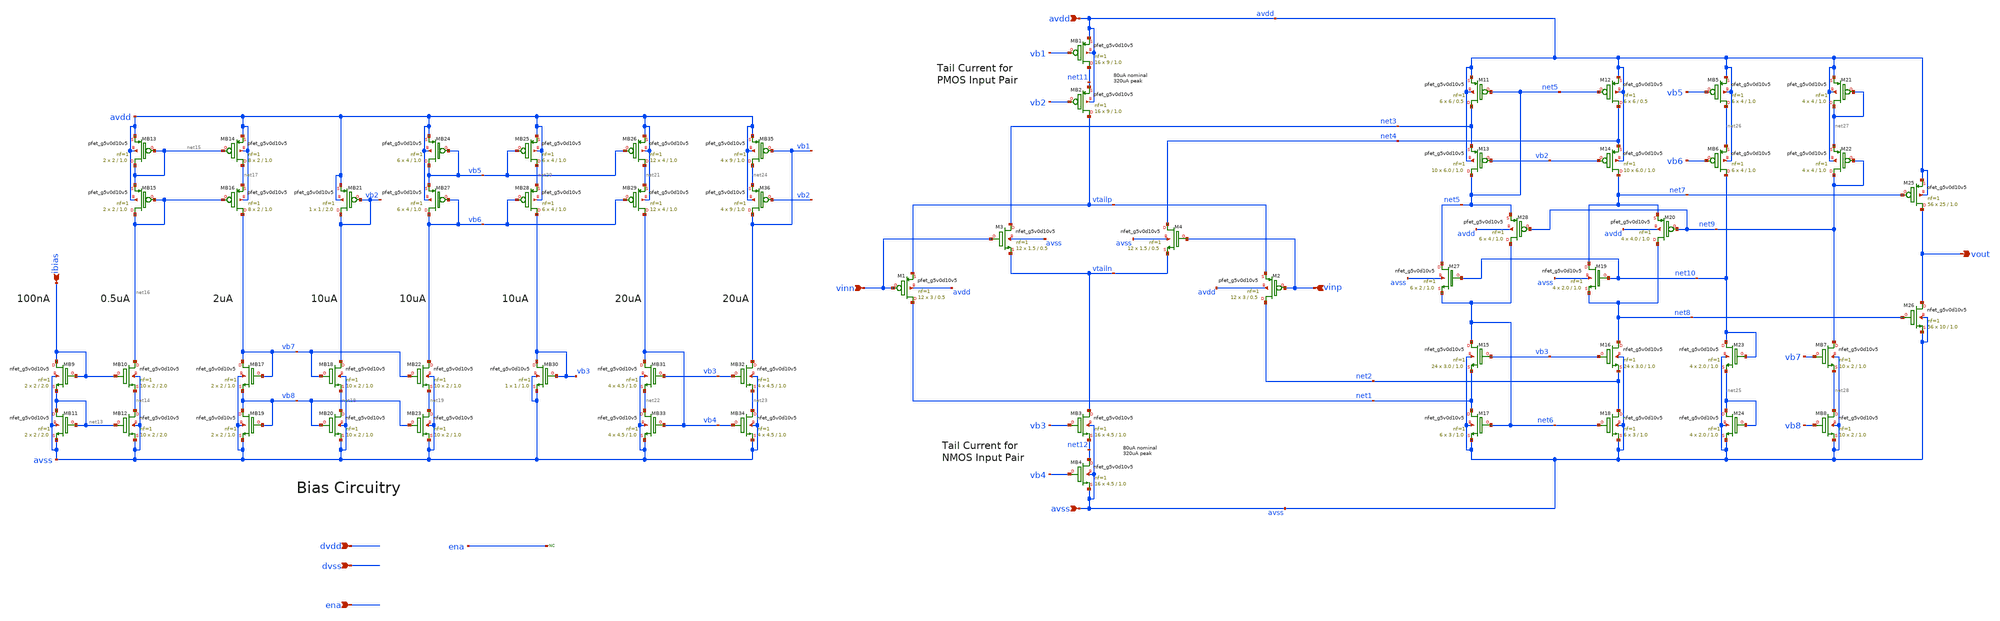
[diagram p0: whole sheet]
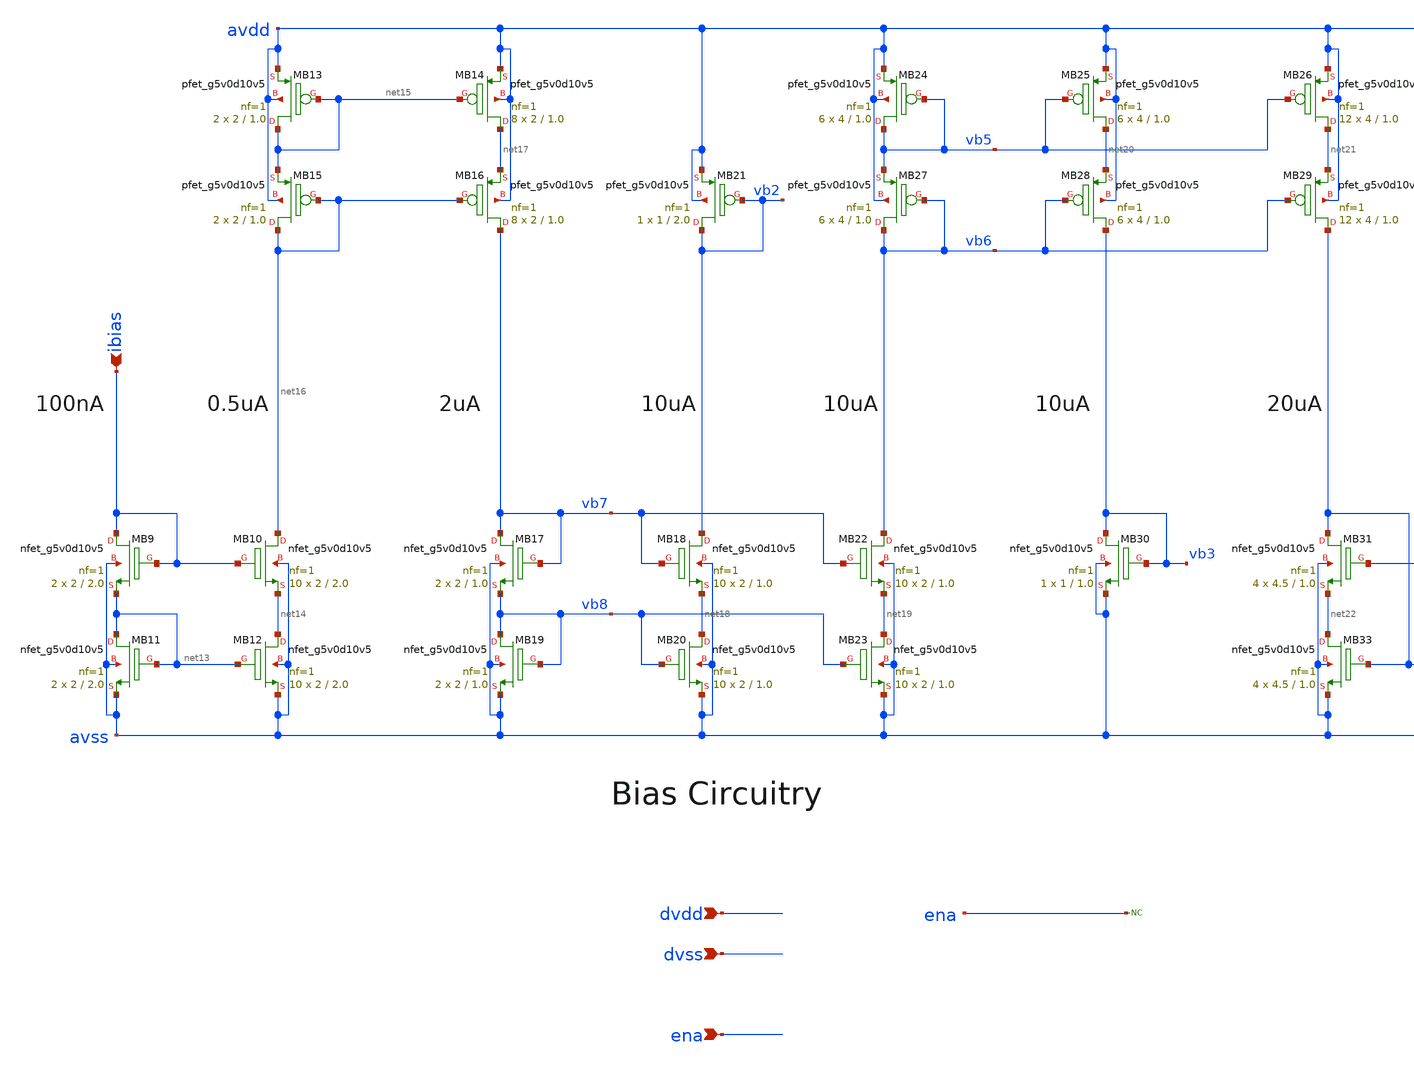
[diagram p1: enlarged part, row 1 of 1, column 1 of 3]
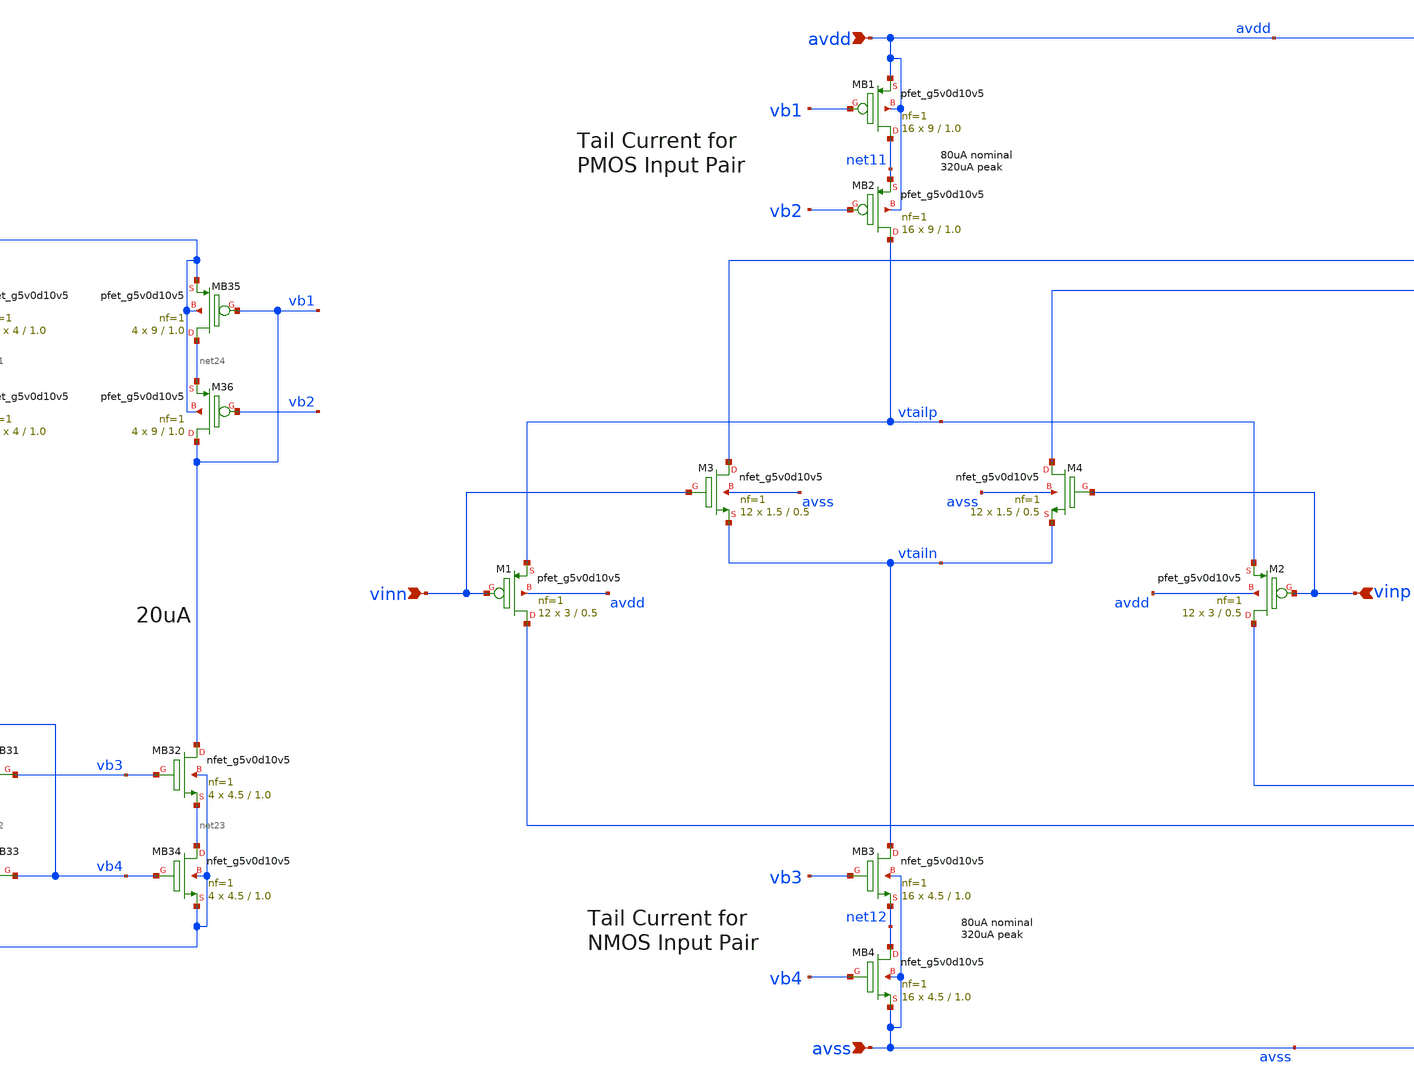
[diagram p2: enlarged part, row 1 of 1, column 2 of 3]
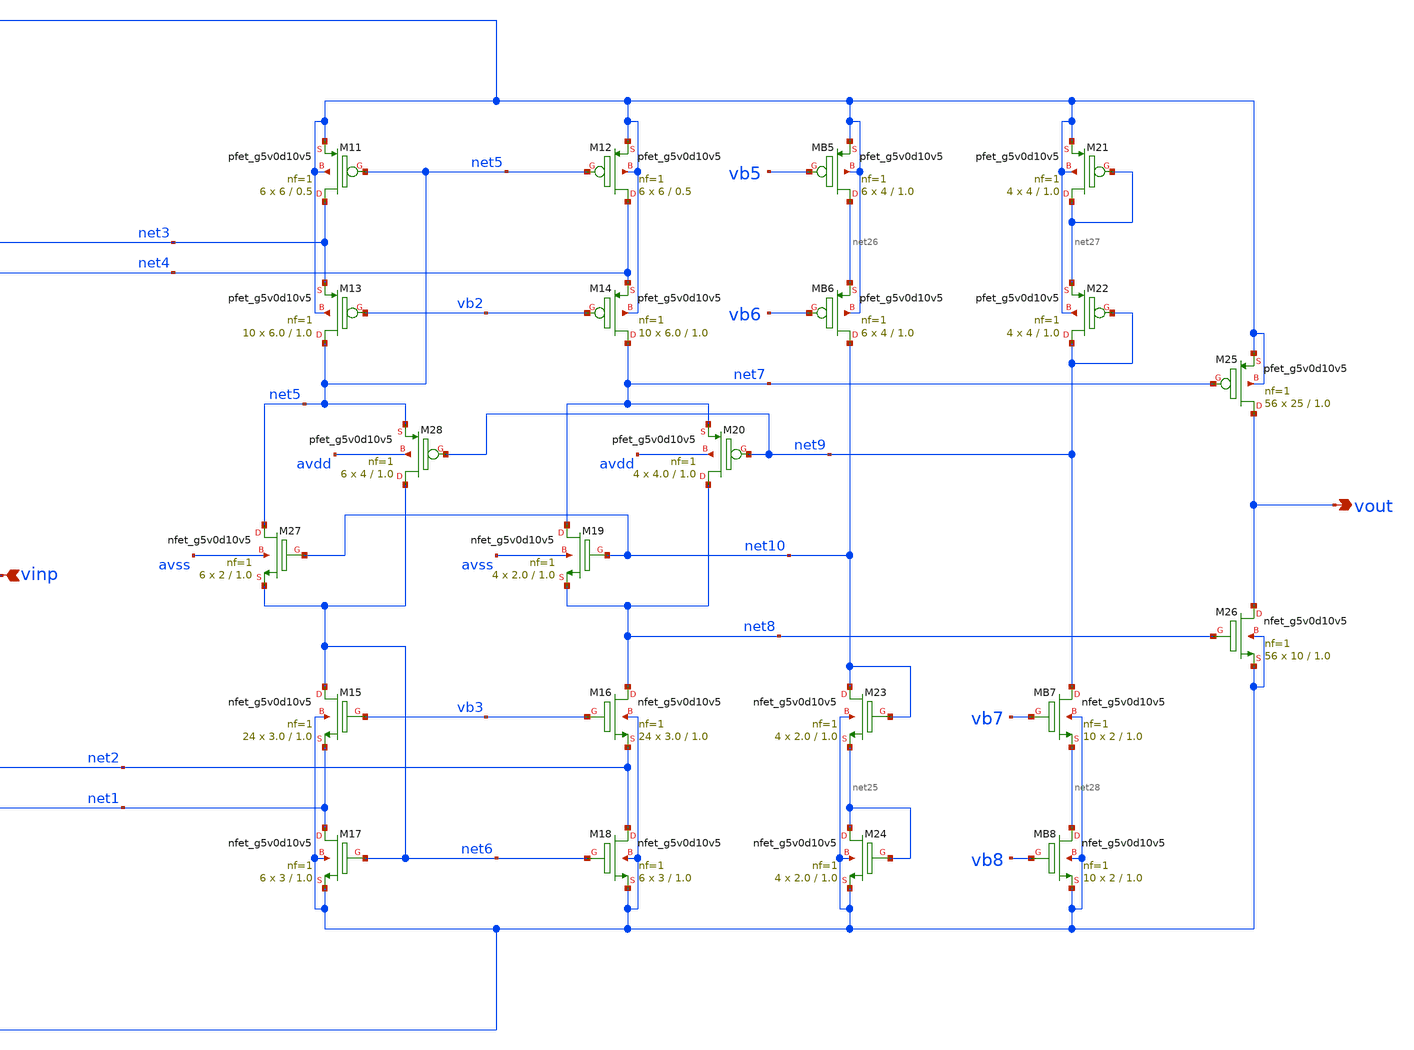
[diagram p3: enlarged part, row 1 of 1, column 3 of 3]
** sch_path: xschem/sky130_td_ip__opamp_hp.sch
**.subckt sky130_td_ip__opamp_hp vinn vinp vout ena ibias avss avdd dvdd dvss
*.ipin vinn
*.ipin vinp
*.opin vout
*.ipin ena
*.ipin ibias
*.ipin avss
*.ipin avdd
*.ipin dvdd
*.ipin dvss
XM3 net3 vinn vtailn avss sky130_fd_pr__nfet_g5v0d10v5 L=0.5 W=1.5 nf=1 ad='int((nf+1)/2) * W/nf * 0.29'
+ as='int((nf+2)/2) * W/nf * 0.29' pd='2*int((nf+1)/2) * (W/nf + 0.29)' ps='2*int((nf+2)/2) * (W/nf + 0.29)'
+ nrd='0.29 / W' nrs='0.29 / W' sa=0 sb=0 sd=0 mult=12 m=12
XM4 net4 vinp vtailn avss sky130_fd_pr__nfet_g5v0d10v5 L=0.5 W=1.5 nf=1 ad='int((nf+1)/2) * W/nf * 0.29'
+ as='int((nf+2)/2) * W/nf * 0.29' pd='2*int((nf+1)/2) * (W/nf + 0.29)' ps='2*int((nf+2)/2) * (W/nf + 0.29)'
+ nrd='0.29 / W' nrs='0.29 / W' sa=0 sb=0 sd=0 mult=12 m=12
XMB3 vtailn vb3 net12 avss sky130_fd_pr__nfet_g5v0d10v5 L=1.0 W=4.5 nf=1 ad='int((nf+1)/2) * W/nf * 0.29'
+ as='int((nf+2)/2) * W/nf * 0.29' pd='2*int((nf+1)/2) * (W/nf + 0.29)' ps='2*int((nf+2)/2) * (W/nf + 0.29)'
+ nrd='0.29 / W' nrs='0.29 / W' sa=0 sb=0 sd=0 mult=16 m=16
XMB4 net12 vb4 avss avss sky130_fd_pr__nfet_g5v0d10v5 L=1.0 W=4.5 nf=1 ad='int((nf+1)/2) * W/nf * 0.29'
+ as='int((nf+2)/2) * W/nf * 0.29' pd='2*int((nf+1)/2) * (W/nf + 0.29)' ps='2*int((nf+2)/2) * (W/nf + 0.29)'
+ nrd='0.29 / W' nrs='0.29 / W' sa=0 sb=0 sd=0 mult=16 m=16
XM1 net1 vinn vtailp avdd sky130_fd_pr__pfet_g5v0d10v5 L=0.5 W=3 nf=1 ad='int((nf+1)/2) * W/nf * 0.29'
+ as='int((nf+2)/2) * W/nf * 0.29' pd='2*int((nf+1)/2) * (W/nf + 0.29)' ps='2*int((nf+2)/2) * (W/nf + 0.29)'
+ nrd='0.29 / W' nrs='0.29 / W' sa=0 sb=0 sd=0 mult=12 m=12
XM2 net2 vinp vtailp avdd sky130_fd_pr__pfet_g5v0d10v5 L=0.5 W=3 nf=1 ad='int((nf+1)/2) * W/nf * 0.29'
+ as='int((nf+2)/2) * W/nf * 0.29' pd='2*int((nf+1)/2) * (W/nf + 0.29)' ps='2*int((nf+2)/2) * (W/nf + 0.29)'
+ nrd='0.29 / W' nrs='0.29 / W' sa=0 sb=0 sd=0 mult=12 m=12
XMB2 vtailp vb2 net11 avdd sky130_fd_pr__pfet_g5v0d10v5 L=1.0 W=9 nf=1 ad='int((nf+1)/2) * W/nf * 0.29'
+ as='int((nf+2)/2) * W/nf * 0.29' pd='2*int((nf+1)/2) * (W/nf + 0.29)' ps='2*int((nf+2)/2) * (W/nf + 0.29)'
+ nrd='0.29 / W' nrs='0.29 / W' sa=0 sb=0 sd=0 mult=16 m=16
XMB1 net11 vb1 avdd avdd sky130_fd_pr__pfet_g5v0d10v5 L=1.0 W=9 nf=1 ad='int((nf+1)/2) * W/nf * 0.29'
+ as='int((nf+2)/2) * W/nf * 0.29' pd='2*int((nf+1)/2) * (W/nf + 0.29)' ps='2*int((nf+2)/2) * (W/nf + 0.29)'
+ nrd='0.29 / W' nrs='0.29 / W' sa=0 sb=0 sd=0 mult=16 m=16
XM12 net4 net5 avdd avdd sky130_fd_pr__pfet_g5v0d10v5 L=0.5 W=6 nf=1 ad='int((nf+1)/2) * W/nf * 0.29'
+ as='int((nf+2)/2) * W/nf * 0.29' pd='2*int((nf+1)/2) * (W/nf + 0.29)' ps='2*int((nf+2)/2) * (W/nf + 0.29)'
+ nrd='0.29 / W' nrs='0.29 / W' sa=0 sb=0 sd=0 mult=6 m=6
XM11 net3 net5 avdd avdd sky130_fd_pr__pfet_g5v0d10v5 L=0.5 W=6 nf=1 ad='int((nf+1)/2) * W/nf * 0.29'
+ as='int((nf+2)/2) * W/nf * 0.29' pd='2*int((nf+1)/2) * (W/nf + 0.29)' ps='2*int((nf+2)/2) * (W/nf + 0.29)'
+ nrd='0.29 / W' nrs='0.29 / W' sa=0 sb=0 sd=0 mult=6 m=6
XM14 net7 vb2 net4 avdd sky130_fd_pr__pfet_g5v0d10v5 L=1.0 W=6.0 nf=1 ad='int((nf+1)/2) * W/nf * 0.29'
+ as='int((nf+2)/2) * W/nf * 0.29' pd='2*int((nf+1)/2) * (W/nf + 0.29)' ps='2*int((nf+2)/2) * (W/nf + 0.29)'
+ nrd='0.29 / W' nrs='0.29 / W' sa=0 sb=0 sd=0 mult=10 m=10
XM13 net5 vb2 net3 avdd sky130_fd_pr__pfet_g5v0d10v5 L=1.0 W=6.0 nf=1 ad='int((nf+1)/2) * W/nf * 0.29'
+ as='int((nf+2)/2) * W/nf * 0.29' pd='2*int((nf+1)/2) * (W/nf + 0.29)' ps='2*int((nf+2)/2) * (W/nf + 0.29)'
+ nrd='0.29 / W' nrs='0.29 / W' sa=0 sb=0 sd=0 mult=10 m=10
XM18 net2 net6 avss avss sky130_fd_pr__nfet_g5v0d10v5 L=1.0 W=3 nf=1 ad='int((nf+1)/2) * W/nf * 0.29'
+ as='int((nf+2)/2) * W/nf * 0.29' pd='2*int((nf+1)/2) * (W/nf + 0.29)' ps='2*int((nf+2)/2) * (W/nf + 0.29)'
+ nrd='0.29 / W' nrs='0.29 / W' sa=0 sb=0 sd=0 mult=6 m=6
XM16 net8 vb3 net2 avss sky130_fd_pr__nfet_g5v0d10v5 L=1.0 W=3.0 nf=1 ad='int((nf+1)/2) * W/nf * 0.29'
+ as='int((nf+2)/2) * W/nf * 0.29' pd='2*int((nf+1)/2) * (W/nf + 0.29)' ps='2*int((nf+2)/2) * (W/nf + 0.29)'
+ nrd='0.29 / W' nrs='0.29 / W' sa=0 sb=0 sd=0 mult=24 m=24
XM17 net1 net6 avss avss sky130_fd_pr__nfet_g5v0d10v5 L=1.0 W=3 nf=1 ad='int((nf+1)/2) * W/nf * 0.29'
+ as='int((nf+2)/2) * W/nf * 0.29' pd='2*int((nf+1)/2) * (W/nf + 0.29)' ps='2*int((nf+2)/2) * (W/nf + 0.29)'
+ nrd='0.29 / W' nrs='0.29 / W' sa=0 sb=0 sd=0 mult=6 m=6
XM15 net6 vb3 net1 avss sky130_fd_pr__nfet_g5v0d10v5 L=1.0 W=3.0 nf=1 ad='int((nf+1)/2) * W/nf * 0.29'
+ as='int((nf+2)/2) * W/nf * 0.29' pd='2*int((nf+1)/2) * (W/nf + 0.29)' ps='2*int((nf+2)/2) * (W/nf + 0.29)'
+ nrd='0.29 / W' nrs='0.29 / W' sa=0 sb=0 sd=0 mult=24 m=24
XM28 net6 net9 net5 avdd sky130_fd_pr__pfet_g5v0d10v5 L=1.0 W=4 nf=1 ad='int((nf+1)/2) * W/nf * 0.29'
+ as='int((nf+2)/2) * W/nf * 0.29' pd='2*int((nf+1)/2) * (W/nf + 0.29)' ps='2*int((nf+2)/2) * (W/nf + 0.29)'
+ nrd='0.29 / W' nrs='0.29 / W' sa=0 sb=0 sd=0 mult=6 m=6
XM27 net5 net10 net6 avss sky130_fd_pr__nfet_g5v0d10v5 L=1.0 W=2 nf=1 ad='int((nf+1)/2) * W/nf * 0.29'
+ as='int((nf+2)/2) * W/nf * 0.29' pd='2*int((nf+1)/2) * (W/nf + 0.29)' ps='2*int((nf+2)/2) * (W/nf + 0.29)'
+ nrd='0.29 / W' nrs='0.29 / W' sa=0 sb=0 sd=0 mult=6 m=6
XM20 net8 net9 net7 avdd sky130_fd_pr__pfet_g5v0d10v5 L=1.0 W=4.0 nf=1 ad='int((nf+1)/2) * W/nf * 0.29'
+ as='int((nf+2)/2) * W/nf * 0.29' pd='2*int((nf+1)/2) * (W/nf + 0.29)' ps='2*int((nf+2)/2) * (W/nf + 0.29)'
+ nrd='0.29 / W' nrs='0.29 / W' sa=0 sb=0 sd=0 mult=4 m=4
XM19 net7 net10 net8 avss sky130_fd_pr__nfet_g5v0d10v5 L=1.0 W=2.0 nf=1 ad='int((nf+1)/2) * W/nf * 0.29'
+ as='int((nf+2)/2) * W/nf * 0.29' pd='2*int((nf+1)/2) * (W/nf + 0.29)' ps='2*int((nf+2)/2) * (W/nf + 0.29)'
+ nrd='0.29 / W' nrs='0.29 / W' sa=0 sb=0 sd=0 mult=4 m=4
XM26 vout net8 avss avss sky130_fd_pr__nfet_g5v0d10v5 L=1.0 W=10 nf=1 ad='int((nf+1)/2) * W/nf * 0.29'
+ as='int((nf+2)/2) * W/nf * 0.29' pd='2*int((nf+1)/2) * (W/nf + 0.29)' ps='2*int((nf+2)/2) * (W/nf + 0.29)'
+ nrd='0.29 / W' nrs='0.29 / W' sa=0 sb=0 sd=0 mult=56 m=56
XM25 vout net7 avdd avdd sky130_fd_pr__pfet_g5v0d10v5 L=1.0 W=25 nf=1 ad='int((nf+1)/2) * W/nf * 0.29'
+ as='int((nf+2)/2) * W/nf * 0.29' pd='2*int((nf+1)/2) * (W/nf + 0.29)' ps='2*int((nf+2)/2) * (W/nf + 0.29)'
+ nrd='0.29 / W' nrs='0.29 / W' sa=0 sb=0 sd=0 mult=56 m=56
XMB9 ibias ibias net13 avss sky130_fd_pr__nfet_g5v0d10v5 L=2.0 W=2 nf=1 ad='int((nf+1)/2) * W/nf * 0.29'
+ as='int((nf+2)/2) * W/nf * 0.29' pd='2*int((nf+1)/2) * (W/nf + 0.29)' ps='2*int((nf+2)/2) * (W/nf + 0.29)'
+ nrd='0.29 / W' nrs='0.29 / W' sa=0 sb=0 sd=0 mult=2 m=2
XMB11 net13 net13 avss avss sky130_fd_pr__nfet_g5v0d10v5 L=2.0 W=2 nf=1 ad='int((nf+1)/2) * W/nf * 0.29'
+ as='int((nf+2)/2) * W/nf * 0.29' pd='2*int((nf+1)/2) * (W/nf + 0.29)' ps='2*int((nf+2)/2) * (W/nf + 0.29)'
+ nrd='0.29 / W' nrs='0.29 / W' sa=0 sb=0 sd=0 mult=2 m=2
XMB10 net16 ibias net14 avss sky130_fd_pr__nfet_g5v0d10v5 L=2.0 W=2 nf=1 ad='int((nf+1)/2) * W/nf * 0.29'
+ as='int((nf+2)/2) * W/nf * 0.29' pd='2*int((nf+1)/2) * (W/nf + 0.29)' ps='2*int((nf+2)/2) * (W/nf + 0.29)'
+ nrd='0.29 / W' nrs='0.29 / W' sa=0 sb=0 sd=0 mult=10 m=10
XMB12 net14 net13 avss avss sky130_fd_pr__nfet_g5v0d10v5 L=2.0 W=2 nf=1 ad='int((nf+1)/2) * W/nf * 0.29'
+ as='int((nf+2)/2) * W/nf * 0.29' pd='2*int((nf+1)/2) * (W/nf + 0.29)' ps='2*int((nf+2)/2) * (W/nf + 0.29)'
+ nrd='0.29 / W' nrs='0.29 / W' sa=0 sb=0 sd=0 mult=10 m=10
XMB15 net16 net16 net15 avdd sky130_fd_pr__pfet_g5v0d10v5 L=1.0 W=2 nf=1 ad='int((nf+1)/2) * W/nf * 0.29'
+ as='int((nf+2)/2) * W/nf * 0.29' pd='2*int((nf+1)/2) * (W/nf + 0.29)' ps='2*int((nf+2)/2) * (W/nf + 0.29)'
+ nrd='0.29 / W' nrs='0.29 / W' sa=0 sb=0 sd=0 mult=2 m=2
XMB13 net15 net15 avdd avdd sky130_fd_pr__pfet_g5v0d10v5 L=1.0 W=2 nf=1 ad='int((nf+1)/2) * W/nf * 0.29'
+ as='int((nf+2)/2) * W/nf * 0.29' pd='2*int((nf+1)/2) * (W/nf + 0.29)' ps='2*int((nf+2)/2) * (W/nf + 0.29)'
+ nrd='0.29 / W' nrs='0.29 / W' sa=0 sb=0 sd=0 mult=2 m=2
XMB16 vb7 net16 net17 avdd sky130_fd_pr__pfet_g5v0d10v5 L=1.0 W=2 nf=1 ad='int((nf+1)/2) * W/nf * 0.29'
+ as='int((nf+2)/2) * W/nf * 0.29' pd='2*int((nf+1)/2) * (W/nf + 0.29)' ps='2*int((nf+2)/2) * (W/nf + 0.29)'
+ nrd='0.29 / W' nrs='0.29 / W' sa=0 sb=0 sd=0 mult=8 m=8
XMB14 net17 net15 avdd avdd sky130_fd_pr__pfet_g5v0d10v5 L=1.0 W=2 nf=1 ad='int((nf+1)/2) * W/nf * 0.29'
+ as='int((nf+2)/2) * W/nf * 0.29' pd='2*int((nf+1)/2) * (W/nf + 0.29)' ps='2*int((nf+2)/2) * (W/nf + 0.29)'
+ nrd='0.29 / W' nrs='0.29 / W' sa=0 sb=0 sd=0 mult=8 m=8
XMB17 vb7 vb7 vb8 avss sky130_fd_pr__nfet_g5v0d10v5 L=1.0 W=2 nf=1 ad='int((nf+1)/2) * W/nf * 0.29' as='int((nf+2)/2) * W/nf * 0.29'
+ pd='2*int((nf+1)/2) * (W/nf + 0.29)' ps='2*int((nf+2)/2) * (W/nf + 0.29)' nrd='0.29 / W' nrs='0.29 / W'
+ sa=0 sb=0 sd=0 mult=2 m=2
XMB19 vb8 vb8 avss avss sky130_fd_pr__nfet_g5v0d10v5 L=1.0 W=2 nf=1 ad='int((nf+1)/2) * W/nf * 0.29'
+ as='int((nf+2)/2) * W/nf * 0.29' pd='2*int((nf+1)/2) * (W/nf + 0.29)' ps='2*int((nf+2)/2) * (W/nf + 0.29)'
+ nrd='0.29 / W' nrs='0.29 / W' sa=0 sb=0 sd=0 mult=2 m=2
XMB18 vb2 vb7 net18 avss sky130_fd_pr__nfet_g5v0d10v5 L=1.0 W=2 nf=1 ad='int((nf+1)/2) * W/nf * 0.29'
+ as='int((nf+2)/2) * W/nf * 0.29' pd='2*int((nf+1)/2) * (W/nf + 0.29)' ps='2*int((nf+2)/2) * (W/nf + 0.29)'
+ nrd='0.29 / W' nrs='0.29 / W' sa=0 sb=0 sd=0 mult=10 m=10
XMB20 net18 vb8 avss avss sky130_fd_pr__nfet_g5v0d10v5 L=1.0 W=2 nf=1 ad='int((nf+1)/2) * W/nf * 0.29'
+ as='int((nf+2)/2) * W/nf * 0.29' pd='2*int((nf+1)/2) * (W/nf + 0.29)' ps='2*int((nf+2)/2) * (W/nf + 0.29)'
+ nrd='0.29 / W' nrs='0.29 / W' sa=0 sb=0 sd=0 mult=10 m=10
XMB22 vb6 vb7 net19 avss sky130_fd_pr__nfet_g5v0d10v5 L=1.0 W=2 nf=1 ad='int((nf+1)/2) * W/nf * 0.29'
+ as='int((nf+2)/2) * W/nf * 0.29' pd='2*int((nf+1)/2) * (W/nf + 0.29)' ps='2*int((nf+2)/2) * (W/nf + 0.29)'
+ nrd='0.29 / W' nrs='0.29 / W' sa=0 sb=0 sd=0 mult=10 m=10
XMB23 net19 vb8 avss avss sky130_fd_pr__nfet_g5v0d10v5 L=1.0 W=2 nf=1 ad='int((nf+1)/2) * W/nf * 0.29'
+ as='int((nf+2)/2) * W/nf * 0.29' pd='2*int((nf+1)/2) * (W/nf + 0.29)' ps='2*int((nf+2)/2) * (W/nf + 0.29)'
+ nrd='0.29 / W' nrs='0.29 / W' sa=0 sb=0 sd=0 mult=10 m=10
XMB21 vb2 vb2 avdd avdd sky130_fd_pr__pfet_g5v0d10v5 L=2.0 W=1 nf=1 ad='int((nf+1)/2) * W/nf * 0.29'
+ as='int((nf+2)/2) * W/nf * 0.29' pd='2*int((nf+1)/2) * (W/nf + 0.29)' ps='2*int((nf+2)/2) * (W/nf + 0.29)'
+ nrd='0.29 / W' nrs='0.29 / W' sa=0 sb=0 sd=0 mult=1 m=1
XMB27 vb6 vb6 vb5 avdd sky130_fd_pr__pfet_g5v0d10v5 L=1.0 W=4 nf=1 ad='int((nf+1)/2) * W/nf * 0.29' as='int((nf+2)/2) * W/nf * 0.29'
+ pd='2*int((nf+1)/2) * (W/nf + 0.29)' ps='2*int((nf+2)/2) * (W/nf + 0.29)' nrd='0.29 / W' nrs='0.29 / W'
+ sa=0 sb=0 sd=0 mult=6 m=6
XMB24 vb5 vb5 avdd avdd sky130_fd_pr__pfet_g5v0d10v5 L=1.0 W=4 nf=1 ad='int((nf+1)/2) * W/nf * 0.29'
+ as='int((nf+2)/2) * W/nf * 0.29' pd='2*int((nf+1)/2) * (W/nf + 0.29)' ps='2*int((nf+2)/2) * (W/nf + 0.29)'
+ nrd='0.29 / W' nrs='0.29 / W' sa=0 sb=0 sd=0 mult=6 m=6
XMB28 vb3 vb6 net20 avdd sky130_fd_pr__pfet_g5v0d10v5 L=1.0 W=4 nf=1 ad='int((nf+1)/2) * W/nf * 0.29'
+ as='int((nf+2)/2) * W/nf * 0.29' pd='2*int((nf+1)/2) * (W/nf + 0.29)' ps='2*int((nf+2)/2) * (W/nf + 0.29)'
+ nrd='0.29 / W' nrs='0.29 / W' sa=0 sb=0 sd=0 mult=6 m=6
XMB25 net20 vb5 avdd avdd sky130_fd_pr__pfet_g5v0d10v5 L=1.0 W=4 nf=1 ad='int((nf+1)/2) * W/nf * 0.29'
+ as='int((nf+2)/2) * W/nf * 0.29' pd='2*int((nf+1)/2) * (W/nf + 0.29)' ps='2*int((nf+2)/2) * (W/nf + 0.29)'
+ nrd='0.29 / W' nrs='0.29 / W' sa=0 sb=0 sd=0 mult=6 m=6
XMB29 vb4 vb6 net21 avdd sky130_fd_pr__pfet_g5v0d10v5 L=1.0 W=4 nf=1 ad='int((nf+1)/2) * W/nf * 0.29'
+ as='int((nf+2)/2) * W/nf * 0.29' pd='2*int((nf+1)/2) * (W/nf + 0.29)' ps='2*int((nf+2)/2) * (W/nf + 0.29)'
+ nrd='0.29 / W' nrs='0.29 / W' sa=0 sb=0 sd=0 mult=12 m=12
XMB26 net21 vb5 avdd avdd sky130_fd_pr__pfet_g5v0d10v5 L=1.0 W=4 nf=1 ad='int((nf+1)/2) * W/nf * 0.29'
+ as='int((nf+2)/2) * W/nf * 0.29' pd='2*int((nf+1)/2) * (W/nf + 0.29)' ps='2*int((nf+2)/2) * (W/nf + 0.29)'
+ nrd='0.29 / W' nrs='0.29 / W' sa=0 sb=0 sd=0 mult=12 m=12
XMB30 vb3 vb3 avss avss sky130_fd_pr__nfet_g5v0d10v5 L=1.0 W=1 nf=1 ad='int((nf+1)/2) * W/nf * 0.29'
+ as='int((nf+2)/2) * W/nf * 0.29' pd='2*int((nf+1)/2) * (W/nf + 0.29)' ps='2*int((nf+2)/2) * (W/nf + 0.29)'
+ nrd='0.29 / W' nrs='0.29 / W' sa=0 sb=0 sd=0 mult=1 m=1
XMB31 vb4 vb3 net22 avss sky130_fd_pr__nfet_g5v0d10v5 L=1.0 W=4.5 nf=1 ad='int((nf+1)/2) * W/nf * 0.29'
+ as='int((nf+2)/2) * W/nf * 0.29' pd='2*int((nf+1)/2) * (W/nf + 0.29)' ps='2*int((nf+2)/2) * (W/nf + 0.29)'
+ nrd='0.29 / W' nrs='0.29 / W' sa=0 sb=0 sd=0 mult=4 m=4
XMB33 net22 vb4 avss avss sky130_fd_pr__nfet_g5v0d10v5 L=1.0 W=4.5 nf=1 ad='int((nf+1)/2) * W/nf * 0.29'
+ as='int((nf+2)/2) * W/nf * 0.29' pd='2*int((nf+1)/2) * (W/nf + 0.29)' ps='2*int((nf+2)/2) * (W/nf + 0.29)'
+ nrd='0.29 / W' nrs='0.29 / W' sa=0 sb=0 sd=0 mult=4 m=4
XMB32 vb1 vb3 net23 avss sky130_fd_pr__nfet_g5v0d10v5 L=1.0 W=4.5 nf=1 ad='int((nf+1)/2) * W/nf * 0.29'
+ as='int((nf+2)/2) * W/nf * 0.29' pd='2*int((nf+1)/2) * (W/nf + 0.29)' ps='2*int((nf+2)/2) * (W/nf + 0.29)'
+ nrd='0.29 / W' nrs='0.29 / W' sa=0 sb=0 sd=0 mult=4 m=4
XMB34 net23 vb4 avss avss sky130_fd_pr__nfet_g5v0d10v5 L=1.0 W=4.5 nf=1 ad='int((nf+1)/2) * W/nf * 0.29'
+ as='int((nf+2)/2) * W/nf * 0.29' pd='2*int((nf+1)/2) * (W/nf + 0.29)' ps='2*int((nf+2)/2) * (W/nf + 0.29)'
+ nrd='0.29 / W' nrs='0.29 / W' sa=0 sb=0 sd=0 mult=4 m=4
XM36 vb1 vb2 net24 avdd sky130_fd_pr__pfet_g5v0d10v5 L=1.0 W=9 nf=1 ad='int((nf+1)/2) * W/nf * 0.29'
+ as='int((nf+2)/2) * W/nf * 0.29' pd='2*int((nf+1)/2) * (W/nf + 0.29)' ps='2*int((nf+2)/2) * (W/nf + 0.29)'
+ nrd='0.29 / W' nrs='0.29 / W' sa=0 sb=0 sd=0 mult=4 m=4
XMB35 net24 vb1 avdd avdd sky130_fd_pr__pfet_g5v0d10v5 L=1.0 W=9 nf=1 ad='int((nf+1)/2) * W/nf * 0.29'
+ as='int((nf+2)/2) * W/nf * 0.29' pd='2*int((nf+1)/2) * (W/nf + 0.29)' ps='2*int((nf+2)/2) * (W/nf + 0.29)'
+ nrd='0.29 / W' nrs='0.29 / W' sa=0 sb=0 sd=0 mult=4 m=4
XM24 net25 net25 avss avss sky130_fd_pr__nfet_g5v0d10v5 L=1.0 W=2.0 nf=1 ad='int((nf+1)/2) * W/nf * 0.29'
+ as='int((nf+2)/2) * W/nf * 0.29' pd='2*int((nf+1)/2) * (W/nf + 0.29)' ps='2*int((nf+2)/2) * (W/nf + 0.29)'
+ nrd='0.29 / W' nrs='0.29 / W' sa=0 sb=0 sd=0 mult=4 m=4
XM23 net10 net10 net25 avss sky130_fd_pr__nfet_g5v0d10v5 L=1.0 W=2.0 nf=1 ad='int((nf+1)/2) * W/nf * 0.29'
+ as='int((nf+2)/2) * W/nf * 0.29' pd='2*int((nf+1)/2) * (W/nf + 0.29)' ps='2*int((nf+2)/2) * (W/nf + 0.29)'
+ nrd='0.29 / W' nrs='0.29 / W' sa=0 sb=0 sd=0 mult=4 m=4
XMB5 net26 vb5 avdd avdd sky130_fd_pr__pfet_g5v0d10v5 L=1.0 W=4 nf=1 ad='int((nf+1)/2) * W/nf * 0.29'
+ as='int((nf+2)/2) * W/nf * 0.29' pd='2*int((nf+1)/2) * (W/nf + 0.29)' ps='2*int((nf+2)/2) * (W/nf + 0.29)'
+ nrd='0.29 / W' nrs='0.29 / W' sa=0 sb=0 sd=0 mult=6 m=6
XMB6 net10 vb6 net26 avdd sky130_fd_pr__pfet_g5v0d10v5 L=1.0 W=4 nf=1 ad='int((nf+1)/2) * W/nf * 0.29'
+ as='int((nf+2)/2) * W/nf * 0.29' pd='2*int((nf+1)/2) * (W/nf + 0.29)' ps='2*int((nf+2)/2) * (W/nf + 0.29)'
+ nrd='0.29 / W' nrs='0.29 / W' sa=0 sb=0 sd=0 mult=6 m=6
XM21 net27 net27 avdd avdd sky130_fd_pr__pfet_g5v0d10v5 L=1.0 W=4 nf=1 ad='int((nf+1)/2) * W/nf * 0.29'
+ as='int((nf+2)/2) * W/nf * 0.29' pd='2*int((nf+1)/2) * (W/nf + 0.29)' ps='2*int((nf+2)/2) * (W/nf + 0.29)'
+ nrd='0.29 / W' nrs='0.29 / W' sa=0 sb=0 sd=0 mult=4 m=4
XM22 net9 net9 net27 avdd sky130_fd_pr__pfet_g5v0d10v5 L=1.0 W=4 nf=1 ad='int((nf+1)/2) * W/nf * 0.29'
+ as='int((nf+2)/2) * W/nf * 0.29' pd='2*int((nf+1)/2) * (W/nf + 0.29)' ps='2*int((nf+2)/2) * (W/nf + 0.29)'
+ nrd='0.29 / W' nrs='0.29 / W' sa=0 sb=0 sd=0 mult=4 m=4
XMB8 net28 vb8 avss avss sky130_fd_pr__nfet_g5v0d10v5 L=1.0 W=2 nf=1 ad='int((nf+1)/2) * W/nf * 0.29'
+ as='int((nf+2)/2) * W/nf * 0.29' pd='2*int((nf+1)/2) * (W/nf + 0.29)' ps='2*int((nf+2)/2) * (W/nf + 0.29)'
+ nrd='0.29 / W' nrs='0.29 / W' sa=0 sb=0 sd=0 mult=10 m=10
XMB7 net9 vb7 net28 avss sky130_fd_pr__nfet_g5v0d10v5 L=1.0 W=2 nf=1 ad='int((nf+1)/2) * W/nf * 0.29'
+ as='int((nf+2)/2) * W/nf * 0.29' pd='2*int((nf+1)/2) * (W/nf + 0.29)' ps='2*int((nf+2)/2) * (W/nf + 0.29)'
+ nrd='0.29 / W' nrs='0.29 / W' sa=0 sb=0 sd=0 mult=10 m=10
* noconn ena
**.ends
.end
